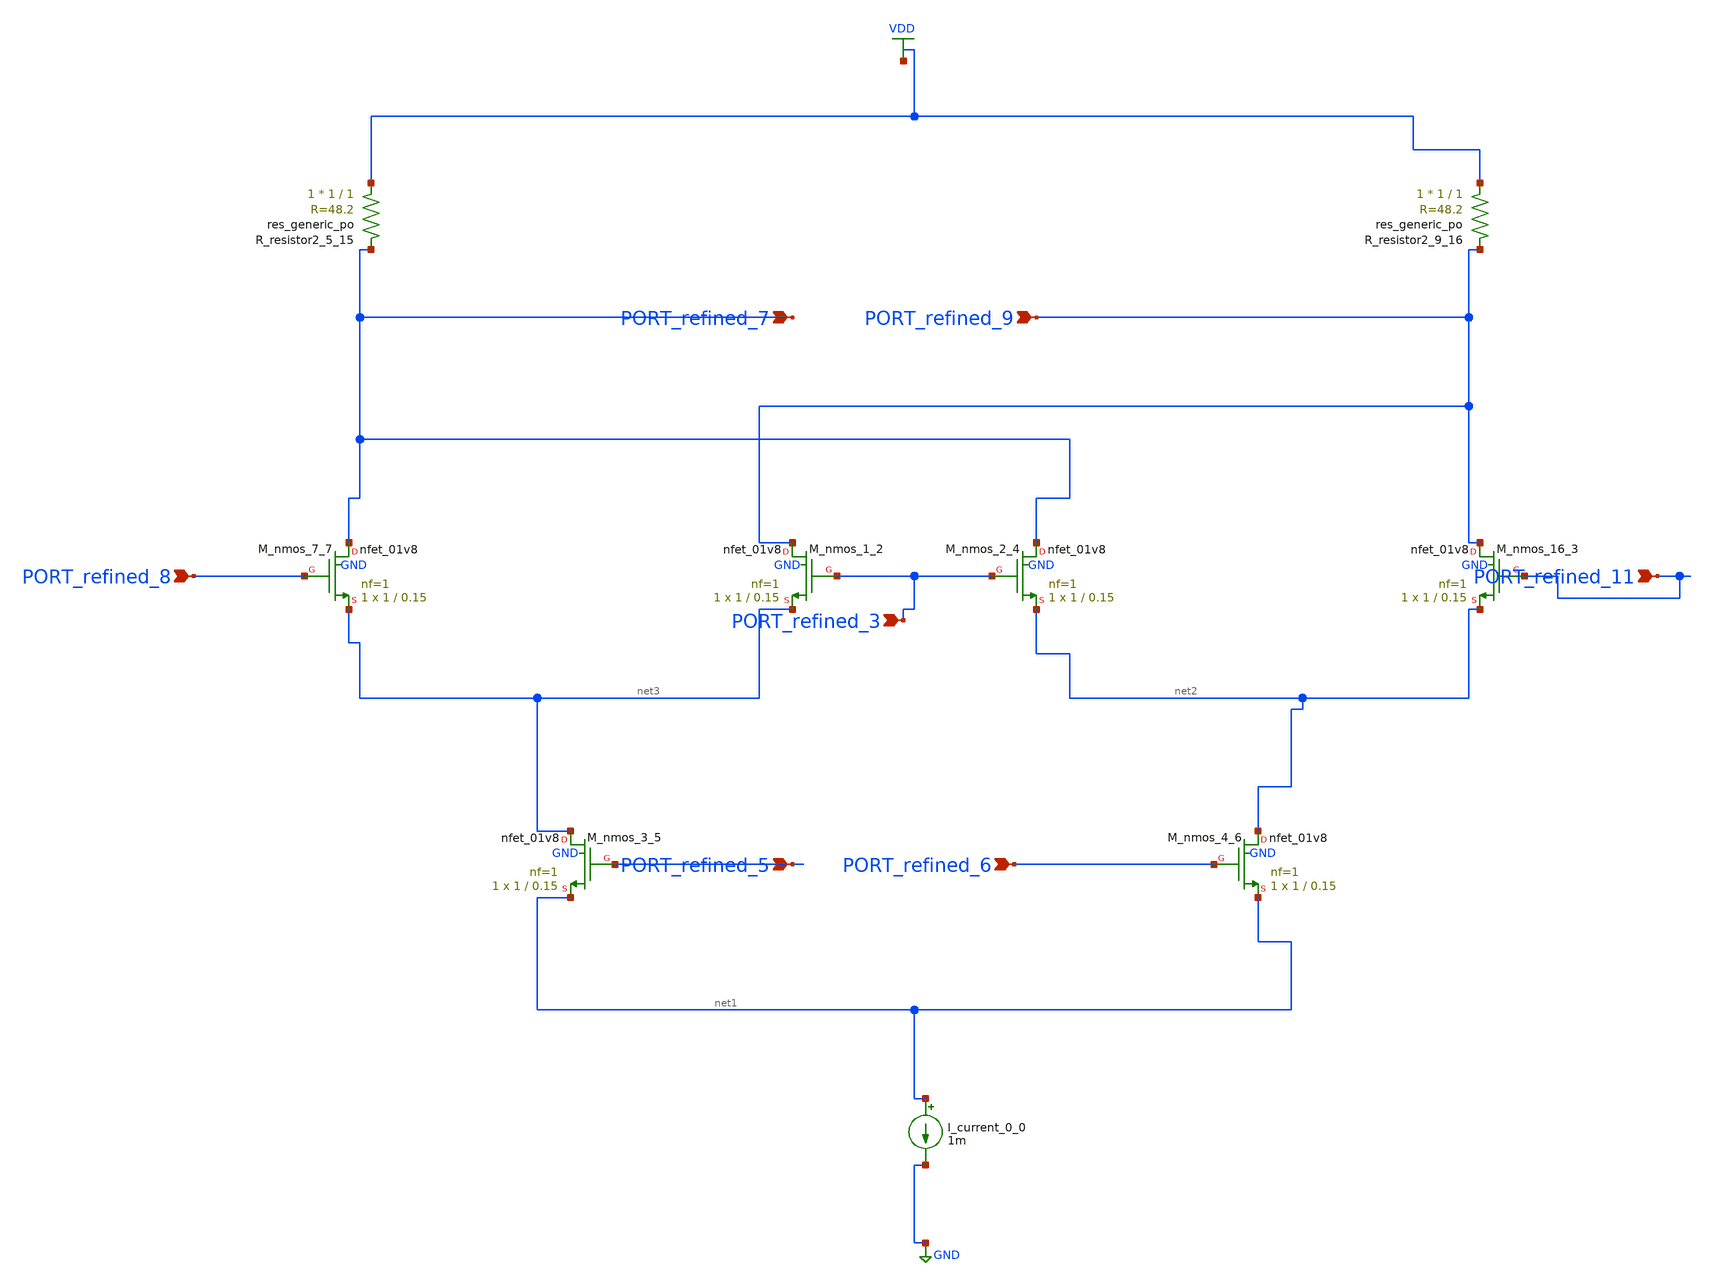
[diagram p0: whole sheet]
** sch_path: schematics/10_29292_jics_v17i1_583_03_003_crop1.sch
**.subckt 10_29292_jics_v17i1_583_03_003_crop1 PORT_refined_6 PORT_refined_7 PORT_refined_5
*+ PORT_refined_9 PORT_refined_8 PORT_refined_11 PORT_refined_3
*.ipin PORT_refined_6
*.ipin PORT_refined_7
*.ipin PORT_refined_5
*.ipin PORT_refined_9
*.ipin PORT_refined_8
*.ipin PORT_refined_11
*.ipin PORT_refined_3
I_current_0_0 net1 GND 1m
XM_nmos_1_2 PORT_refined_9 PORT_refined_3 net3 GND sky130_fd_pr__nfet_01v8 L=0.15 W=1 nf=1 ad='int((1 + 1)/2) * 1 / 1 * 0.29'
+ as='int((1 + 2)/2) * 1 / 1 * 0.29' pd='2*int((1 + 1)/2) * (1 / 1 + 0.29)' ps='2*int((1 + 2)/2) * (1 / 1 + 0.29)'
+ nrd='0.29 / 1 ' nrs='0.29 / 1 ' sa=0 sb=0 sd=0 mult=1 m=1
XM_nmos_16_3 PORT_refined_9 PORT_refined_11 net2 GND sky130_fd_pr__nfet_01v8 L=0.15 W=1 nf=1 ad='int((1 + 1)/2) * 1 / 1 * 0.29'
+ as='int((1 + 2)/2) * 1 / 1 * 0.29' pd='2*int((1 + 1)/2) * (1 / 1 + 0.29)' ps='2*int((1 + 2)/2) * (1 / 1 + 0.29)'
+ nrd='0.29 / 1 ' nrs='0.29 / 1 ' sa=0 sb=0 sd=0 mult=1 m=1
XM_nmos_2_4 PORT_refined_7 PORT_refined_3 net2 GND sky130_fd_pr__nfet_01v8 L=0.15 W=1 nf=1 ad='int((1 + 1)/2) * 1 / 1 * 0.29'
+ as='int((1 + 2)/2) * 1 / 1 * 0.29' pd='2*int((1 + 1)/2) * (1 / 1 + 0.29)' ps='2*int((1 + 2)/2) * (1 / 1 + 0.29)'
+ nrd='0.29 / 1 ' nrs='0.29 / 1 ' sa=0 sb=0 sd=0 mult=1 m=1
XM_nmos_3_5 net3 PORT_refined_5 net1 GND sky130_fd_pr__nfet_01v8 L=0.15 W=1 nf=1 ad='int((1 + 1)/2) * 1 / 1 * 0.29'
+ as='int((1 + 2)/2) * 1 / 1 * 0.29' pd='2*int((1 + 1)/2) * (1 / 1 + 0.29)' ps='2*int((1 + 2)/2) * (1 / 1 + 0.29)'
+ nrd='0.29 / 1 ' nrs='0.29 / 1 ' sa=0 sb=0 sd=0 mult=1 m=1
XM_nmos_4_6 net2 PORT_refined_6 net1 GND sky130_fd_pr__nfet_01v8 L=0.15 W=1 nf=1 ad='int((1 + 1)/2) * 1 / 1 * 0.29'
+ as='int((1 + 2)/2) * 1 / 1 * 0.29' pd='2*int((1 + 1)/2) * (1 / 1 + 0.29)' ps='2*int((1 + 2)/2) * (1 / 1 + 0.29)'
+ nrd='0.29 / 1 ' nrs='0.29 / 1 ' sa=0 sb=0 sd=0 mult=1 m=1
XM_nmos_7_7 PORT_refined_7 PORT_refined_8 net3 GND sky130_fd_pr__nfet_01v8 L=0.15 W=1 nf=1 ad='int((1 + 1)/2) * 1 / 1 * 0.29'
+ as='int((1 + 2)/2) * 1 / 1 * 0.29' pd='2*int((1 + 1)/2) * (1 / 1 + 0.29)' ps='2*int((1 + 2)/2) * (1 / 1 + 0.29)'
+ nrd='0.29 / 1 ' nrs='0.29 / 1 ' sa=0 sb=0 sd=0 mult=1 m=1
XR_resistor2_5_15 VDD PORT_refined_7 sky130_fd_pr__res_generic_po W=1 L=1 m=1
XR_resistor2_9_16 VDD PORT_refined_9 sky130_fd_pr__res_generic_po W=1 L=1 m=1
**.ends
.GLOBAL GND
.GLOBAL VDD
.end
